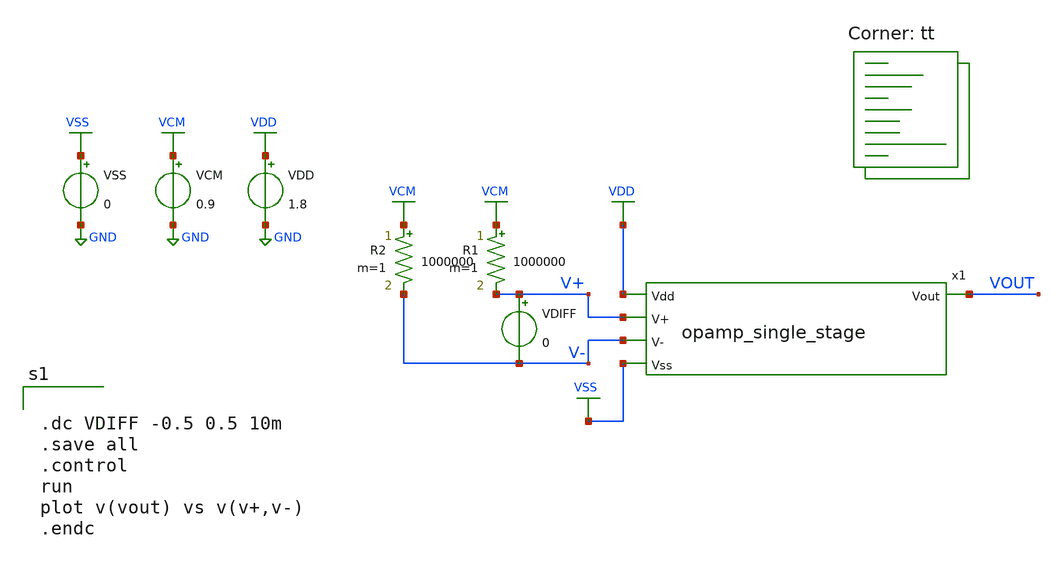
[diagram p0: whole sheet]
** sch_path: analog/schematics/tb_dc_analysis.sch
**.subckt tb_dc_analysis
VDD VDD GND 1.8
VCM VCM GND 0.9
R1 VCM V+ 1000000 m=1
R2 VCM V- 1000000 m=1
VSS VSS GND 0
VDIFF V+ V- 0
x1 VDD VOUT V+ V- VSS opamp_single_stage
**** begin user architecture code


.dc VDIFF -0.5 0.5 10m
.save all
.control
run
plot v(vout) vs v(v+,v-)
.endc


.lib $::SKYWATER_MODELS/sky130.lib.spice tt
**** end user architecture code
**.ends

* expanding   symbol:  opamp_single_stage.sym # of pins=5
** sym_path: analog/schematics/opamp_single_stage.sym
** sch_path: analog/schematics/opamp_single_stage.sch
.subckt opamp_single_stage Vdd Vout V+ V- Vss
*.opin Vout
*.ipin Vdd
*.ipin Vss
*.ipin V+
*.ipin V-
XM3 net1 V+ net2 Vss sky130_fd_pr__nfet_01v8 L=0.25 W=1 nf=1 ad='int((nf+1)/2) * W/nf * 0.29' as='int((nf+2)/2) * W/nf * 0.29'
+ pd='2*int((nf+1)/2) * (W/nf + 0.29)' ps='2*int((nf+2)/2) * (W/nf + 0.29)' nrd='0.29 / W' nrs='0.29 / W'
+ sa=0 sb=0 sd=0 mult=1 m=1
XM4 Vout V- net2 Vss sky130_fd_pr__nfet_01v8 L=0.25 W=1 nf=1 ad='int((nf+1)/2) * W/nf * 0.29' as='int((nf+2)/2) * W/nf * 0.29'
+ pd='2*int((nf+1)/2) * (W/nf + 0.29)' ps='2*int((nf+2)/2) * (W/nf + 0.29)' nrd='0.29 / W' nrs='0.29 / W'
+ sa=0 sb=0 sd=0 mult=1 m=1
XM5 net2 net3 Vss Vss sky130_fd_pr__nfet_01v8 L=0.25 W=1 nf=1 ad='int((nf+1)/2) * W/nf * 0.29' as='int((nf+2)/2) * W/nf * 0.29'
+ pd='2*int((nf+1)/2) * (W/nf + 0.29)' ps='2*int((nf+2)/2) * (W/nf + 0.29)' nrd='0.29 / W' nrs='0.29 / W'
+ sa=0 sb=0 sd=0 mult=1 m=1
XM1 net1 net1 Vdd Vdd sky130_fd_pr__pfet_01v8 L=0.25 W=1 nf=1 ad='int((nf+1)/2) * W/nf * 0.29' as='int((nf+2)/2) * W/nf * 0.29'
+ pd='2*int((nf+1)/2) * (W/nf + 0.29)' ps='2*int((nf+2)/2) * (W/nf + 0.29)' nrd='0.29 / W' nrs='0.29 / W'
+ sa=0 sb=0 sd=0 mult=1 m=1
XM2 Vout net1 Vdd Vdd sky130_fd_pr__pfet_01v8 L=0.25 W=1 nf=1 ad='int((nf+1)/2) * W/nf * 0.29' as='int((nf+2)/2) * W/nf * 0.29'
+ pd='2*int((nf+1)/2) * (W/nf + 0.29)' ps='2*int((nf+2)/2) * (W/nf + 0.29)' nrd='0.29 / W' nrs='0.29 / W'
+ sa=0 sb=0 sd=0 mult=1 m=1
XM6 net3 net3 Vss Vss sky130_fd_pr__nfet_01v8 L=0.25 W=1 nf=1 ad='int((nf+1)/2) * W/nf * 0.29' as='int((nf+2)/2) * W/nf * 0.29'
+ pd='2*int((nf+1)/2) * (W/nf + 0.29)' ps='2*int((nf+2)/2) * (W/nf + 0.29)' nrd='0.29 / W' nrs='0.29 / W'
+ sa=0 sb=0 sd=0 mult=1 m=1
XR1 net3 Vdd net4 sky130_fd_pr__res_high_po W=2.5 L=0.1 mult=1 m=1
.ends

.GLOBAL GND
.GLOBAL VDD
.GLOBAL VCM
.GLOBAL VSS
.end
